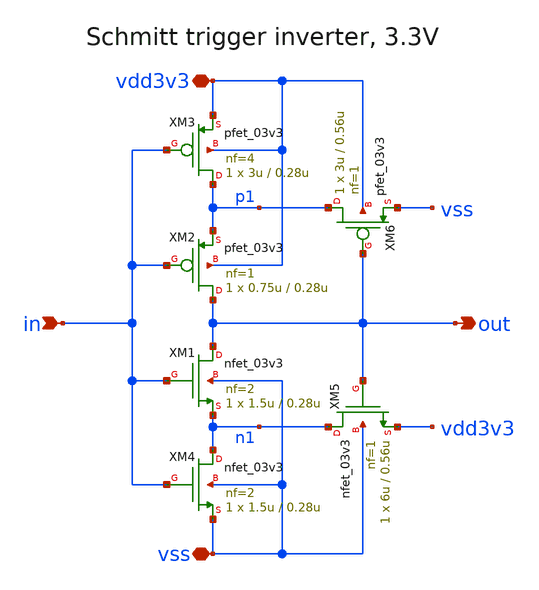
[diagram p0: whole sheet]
** sch_path: projects/programmable_transceiver_platform/analog/core_support/por/xschem/por_3v3_schmitt_inv.sch
**.subckt por_3v3_schmitt_inv vdd3v3 vss in out
*.iopin vdd3v3
*.iopin vss
*.ipin in
*.opin out
XM1 out in n1 vss nfet_03v3 L=0.28u W=1.5u nf=2 ad='int((nf+1)/2) * W/nf * 0.18u' as='int((nf+2)/2) * W/nf * 0.18u'
+ pd='2*int((nf+1)/2) * (W/nf + 0.18u)' ps='2*int((nf+2)/2) * (W/nf + 0.18u)' nrd='0.18u / W' nrs='0.18u / W'
+ sa=0 sb=0 sd=0 m=1
XM2 out in p1 vdd3v3 pfet_03v3 L=0.28u W=0.75u nf=1 ad='int((nf+1)/2) * W/nf * 0.18u' as='int((nf+2)/2) * W/nf * 0.18u'
+ pd='2*int((nf+1)/2) * (W/nf + 0.18u)' ps='2*int((nf+2)/2) * (W/nf + 0.18u)' nrd='0.18u / W' nrs='0.18u / W'
+ sa=0 sb=0 sd=0 m=1
XM3 p1 in vdd3v3 vdd3v3 pfet_03v3 L=0.28u W=3u nf=4 ad='int((nf+1)/2) * W/nf * 0.18u' as='int((nf+2)/2) * W/nf * 0.18u'
+ pd='2*int((nf+1)/2) * (W/nf + 0.18u)' ps='2*int((nf+2)/2) * (W/nf + 0.18u)' nrd='0.18u / W' nrs='0.18u / W'
+ sa=0 sb=0 sd=0 m=1
XM4 n1 in vss vss nfet_03v3 L=0.28u W=1.5u nf=2 ad='int((nf+1)/2) * W/nf * 0.18u' as='int((nf+2)/2) * W/nf * 0.18u'
+ pd='2*int((nf+1)/2) * (W/nf + 0.18u)' ps='2*int((nf+2)/2) * (W/nf + 0.18u)' nrd='0.18u / W' nrs='0.18u / W'
+ sa=0 sb=0 sd=0 m=1
XM5 n1 out vdd3v3 vss nfet_03v3 L=0.56u W=6u nf=1 ad='int((nf+1)/2) * W/nf * 0.18u' as='int((nf+2)/2) * W/nf * 0.18u'
+ pd='2*int((nf+1)/2) * (W/nf + 0.18u)' ps='2*int((nf+2)/2) * (W/nf + 0.18u)' nrd='0.18u / W' nrs='0.18u / W'
+ sa=0 sb=0 sd=0 m=1
XM6 p1 out vss vdd3v3 pfet_03v3 L=0.56u W=3u nf=1 ad='int((nf+1)/2) * W/nf * 0.18u' as='int((nf+2)/2) * W/nf * 0.18u'
+ pd='2*int((nf+1)/2) * (W/nf + 0.18u)' ps='2*int((nf+2)/2) * (W/nf + 0.18u)' nrd='0.18u / W' nrs='0.18u / W'
+ sa=0 sb=0 sd=0 m=1
**.ends
.end
